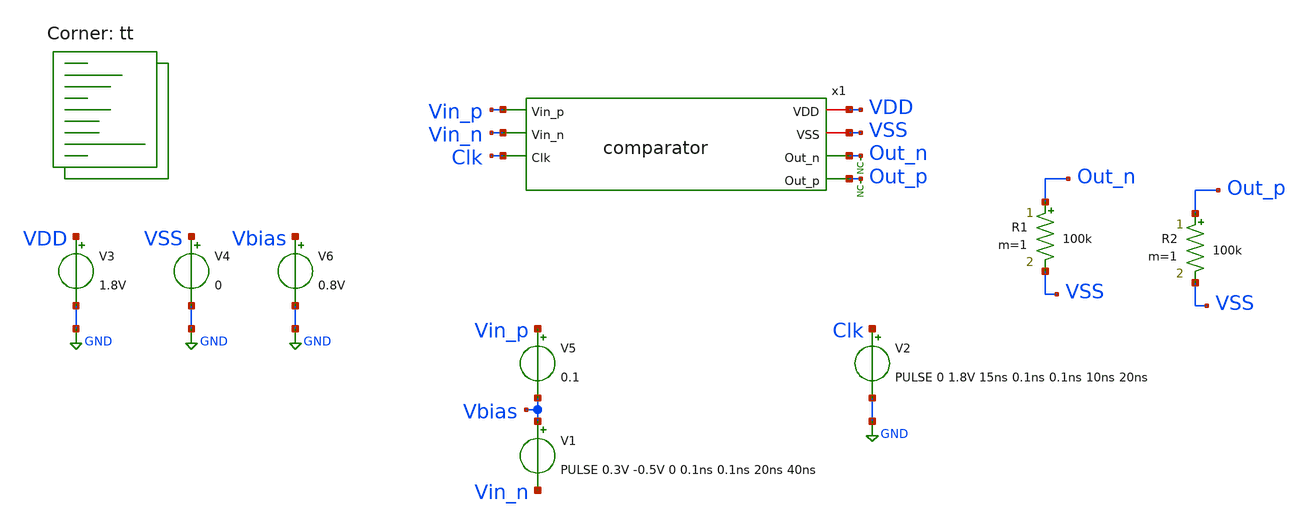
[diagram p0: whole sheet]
** sch_path: xschem/tests/comparator/comparator_fast_large_swing_test.sch
**.subckt comparator_fast_large_swing_test
V3 VDD GND 1.8V
V4 VSS GND 0
V1 Vbias Vin_n PULSE 0.3V -0.5V 0 0.1ns 0.1ns 20ns 40ns
V2 Clk GND PULSE 0 1.8V 15ns 0.1ns 0.1ns 10ns 20ns
* noconn Out_p
* noconn Out_n
V6 Vbias GND 0.8V
R1 Out_n VSS 100k m=1
R2 Out_p VSS 100k m=1
V5 Vin_p Vbias 0.1
x1 VDD VSS Vin_p Out_n Vin_n Out_p Clk comparator
**** begin user architecture code
 *.lib $::SKYWATER_MODELS/sky130.lib.spice tt
.include $::SKYWATER_STDCELLS/sky130_fd_sc_hd.spice


.options acct list
.temp 25
.control
save all
tran 0.1n 170ns
*dc V1 0 1.8V 0.1
plot Vin_p-Vin_n Out_p-Out_n Clk-4
plot Vin_p-Vin_n x1.pre_amp_p-x1.pre_amp_n Clk-4
write comparator_fast_large_swing_test.raw
.endc


.lib $::SKYWATER_MODELS/sky130.lib.spice tt
**** end user architecture code
**.ends

* expanding   symbol:  src/comparator/comparator.sym # of pins=7
** sym_path: xschem/src/comparator/comparator.sym
** sch_path: xschem/src/comparator/comparator.sch
.subckt comparator VDD VSS Vin_p Out_n Vin_n Out_p Clk
*.iopin VDD
*.iopin VSS
*.ipin Vin_p
*.opin Out_n
*.ipin Vin_n
*.opin Out_p
*.ipin Clk
XM1 Pre_Amp_n Clk VDD VSS sky130_fd_pr__pfet_01v8 L=0.15 W=1 nf=1 ad='int((nf+1)/2) * W/nf * 0.29' as='int((nf+2)/2) * W/nf * 0.29'
+ pd='2*int((nf+1)/2) * (W/nf + 0.29)' ps='2*int((nf+2)/2) * (W/nf + 0.29)' nrd='0.29 / W' nrs='0.29 / W'
+ sa=0 sb=0 sd=0 mult=1 m=1
XM2 Pre_Amp_p Clk VDD VSS sky130_fd_pr__pfet_01v8 L=0.15 W=1 nf=1 ad='int((nf+1)/2) * W/nf * 0.29' as='int((nf+2)/2) * W/nf * 0.29'
+ pd='2*int((nf+1)/2) * (W/nf + 0.29)' ps='2*int((nf+2)/2) * (W/nf + 0.29)' nrd='0.29 / W' nrs='0.29 / W'
+ sa=0 sb=0 sd=0 mult=1 m=1
XM3 Pre_Amp_p Vin_p net1 VSS sky130_fd_pr__nfet_01v8 L=0.15 W=1 nf=1 ad='int((nf+1)/2) * W/nf * 0.29'
+ as='int((nf+2)/2) * W/nf * 0.29' pd='2*int((nf+1)/2) * (W/nf + 0.29)' ps='2*int((nf+2)/2) * (W/nf + 0.29)'
+ nrd='0.29 / W' nrs='0.29 / W' sa=0 sb=0 sd=0 mult=1 m=1
XM4 Pre_Amp_n Vin_n net1 VSS sky130_fd_pr__nfet_01v8 L=0.15 W=1 nf=1 ad='int((nf+1)/2) * W/nf * 0.29'
+ as='int((nf+2)/2) * W/nf * 0.29' pd='2*int((nf+1)/2) * (W/nf + 0.29)' ps='2*int((nf+2)/2) * (W/nf + 0.29)'
+ nrd='0.29 / W' nrs='0.29 / W' sa=0 sb=0 sd=0 mult=1 m=1
XM5 net3 Out_p VDD VSS sky130_fd_pr__pfet_01v8 L=0.15 W=1 nf=1 ad='int((nf+1)/2) * W/nf * 0.29' as='int((nf+2)/2) * W/nf * 0.29'
+ pd='2*int((nf+1)/2) * (W/nf + 0.29)' ps='2*int((nf+2)/2) * (W/nf + 0.29)' nrd='0.29 / W' nrs='0.29 / W'
+ sa=0 sb=0 sd=0 mult=1 m=1
XM6 net2 Out_n VDD VSS sky130_fd_pr__pfet_01v8 L=0.15 W=1 nf=1 ad='int((nf+1)/2) * W/nf * 0.29' as='int((nf+2)/2) * W/nf * 0.29'
+ pd='2*int((nf+1)/2) * (W/nf + 0.29)' ps='2*int((nf+2)/2) * (W/nf + 0.29)' nrd='0.29 / W' nrs='0.29 / W'
+ sa=0 sb=0 sd=0 mult=1 m=1
XM7 net2 Pre_Amp_p Out_p VSS sky130_fd_pr__nfet_01v8 L=0.15 W=1 nf=1 ad='int((nf+1)/2) * W/nf * 0.29'
+ as='int((nf+2)/2) * W/nf * 0.29' pd='2*int((nf+1)/2) * (W/nf + 0.29)' ps='2*int((nf+2)/2) * (W/nf + 0.29)'
+ nrd='0.29 / W' nrs='0.29 / W' sa=0 sb=0 sd=0 mult=1 m=1
XM8 net3 Pre_Amp_n Out_n VSS sky130_fd_pr__nfet_01v8 L=0.15 W=1 nf=1 ad='int((nf+1)/2) * W/nf * 0.29'
+ as='int((nf+2)/2) * W/nf * 0.29' pd='2*int((nf+1)/2) * (W/nf + 0.29)' ps='2*int((nf+2)/2) * (W/nf + 0.29)'
+ nrd='0.29 / W' nrs='0.29 / W' sa=0 sb=0 sd=0 mult=1 m=1
XM9 net1 Clk VSS VSS sky130_fd_pr__nfet_01v8 L=0.15 W=1 nf=1 ad='int((nf+1)/2) * W/nf * 0.29' as='int((nf+2)/2) * W/nf * 0.29'
+ pd='2*int((nf+1)/2) * (W/nf + 0.29)' ps='2*int((nf+2)/2) * (W/nf + 0.29)' nrd='0.29 / W' nrs='0.29 / W'
+ sa=0 sb=0 sd=0 mult=1 m=1
XM10 Pre_Amp_n Vin_n net1 VSS sky130_fd_pr__nfet_01v8 L=0.15 W=1 nf=1 ad='int((nf+1)/2) * W/nf * 0.29'
+ as='int((nf+2)/2) * W/nf * 0.29' pd='2*int((nf+1)/2) * (W/nf + 0.29)' ps='2*int((nf+2)/2) * (W/nf + 0.29)'
+ nrd='0.29 / W' nrs='0.29 / W' sa=0 sb=0 sd=0 mult=1 m=1
XM11 Out_n Clk_n VSS VSS sky130_fd_pr__nfet_01v8 L=0.15 W=1 nf=1 ad='int((nf+1)/2) * W/nf * 0.29' as='int((nf+2)/2) * W/nf * 0.29'
+ pd='2*int((nf+1)/2) * (W/nf + 0.29)' ps='2*int((nf+2)/2) * (W/nf + 0.29)' nrd='0.29 / W' nrs='0.29 / W'
+ sa=0 sb=0 sd=0 mult=1 m=1
XM12 Out_n Out_p VSS VSS sky130_fd_pr__nfet_01v8 L=0.15 W=1 nf=1 ad='int((nf+1)/2) * W/nf * 0.29' as='int((nf+2)/2) * W/nf * 0.29'
+ pd='2*int((nf+1)/2) * (W/nf + 0.29)' ps='2*int((nf+2)/2) * (W/nf + 0.29)' nrd='0.29 / W' nrs='0.29 / W'
+ sa=0 sb=0 sd=0 mult=1 m=1
XM13 Out_p Out_n VSS VSS sky130_fd_pr__nfet_01v8 L=0.15 W=1 nf=1 ad='int((nf+1)/2) * W/nf * 0.29' as='int((nf+2)/2) * W/nf * 0.29'
+ pd='2*int((nf+1)/2) * (W/nf + 0.29)' ps='2*int((nf+2)/2) * (W/nf + 0.29)' nrd='0.29 / W' nrs='0.29 / W'
+ sa=0 sb=0 sd=0 mult=1 m=1
XM14 Out_p Clk_n VSS VSS sky130_fd_pr__nfet_01v8 L=0.15 W=1 nf=1 ad='int((nf+1)/2) * W/nf * 0.29' as='int((nf+2)/2) * W/nf * 0.29'
+ pd='2*int((nf+1)/2) * (W/nf + 0.29)' ps='2*int((nf+2)/2) * (W/nf + 0.29)' nrd='0.29 / W' nrs='0.29 / W'
+ sa=0 sb=0 sd=0 mult=1 m=1
XM15 Clk_n Clk VDD VSS sky130_fd_pr__pfet_01v8 L=0.15 W=1 nf=1 ad='int((nf+1)/2) * W/nf * 0.29' as='int((nf+2)/2) * W/nf * 0.29'
+ pd='2*int((nf+1)/2) * (W/nf + 0.29)' ps='2*int((nf+2)/2) * (W/nf + 0.29)' nrd='0.29 / W' nrs='0.29 / W'
+ sa=0 sb=0 sd=0 mult=1 m=1
XM16 Clk_n Clk VSS VSS sky130_fd_pr__nfet_01v8 L=0.15 W=1 nf=1 ad='int((nf+1)/2) * W/nf * 0.29' as='int((nf+2)/2) * W/nf * 0.29'
+ pd='2*int((nf+1)/2) * (W/nf + 0.29)' ps='2*int((nf+2)/2) * (W/nf + 0.29)' nrd='0.29 / W' nrs='0.29 / W'
+ sa=0 sb=0 sd=0 mult=1 m=1
.ends

.GLOBAL GND
.end
